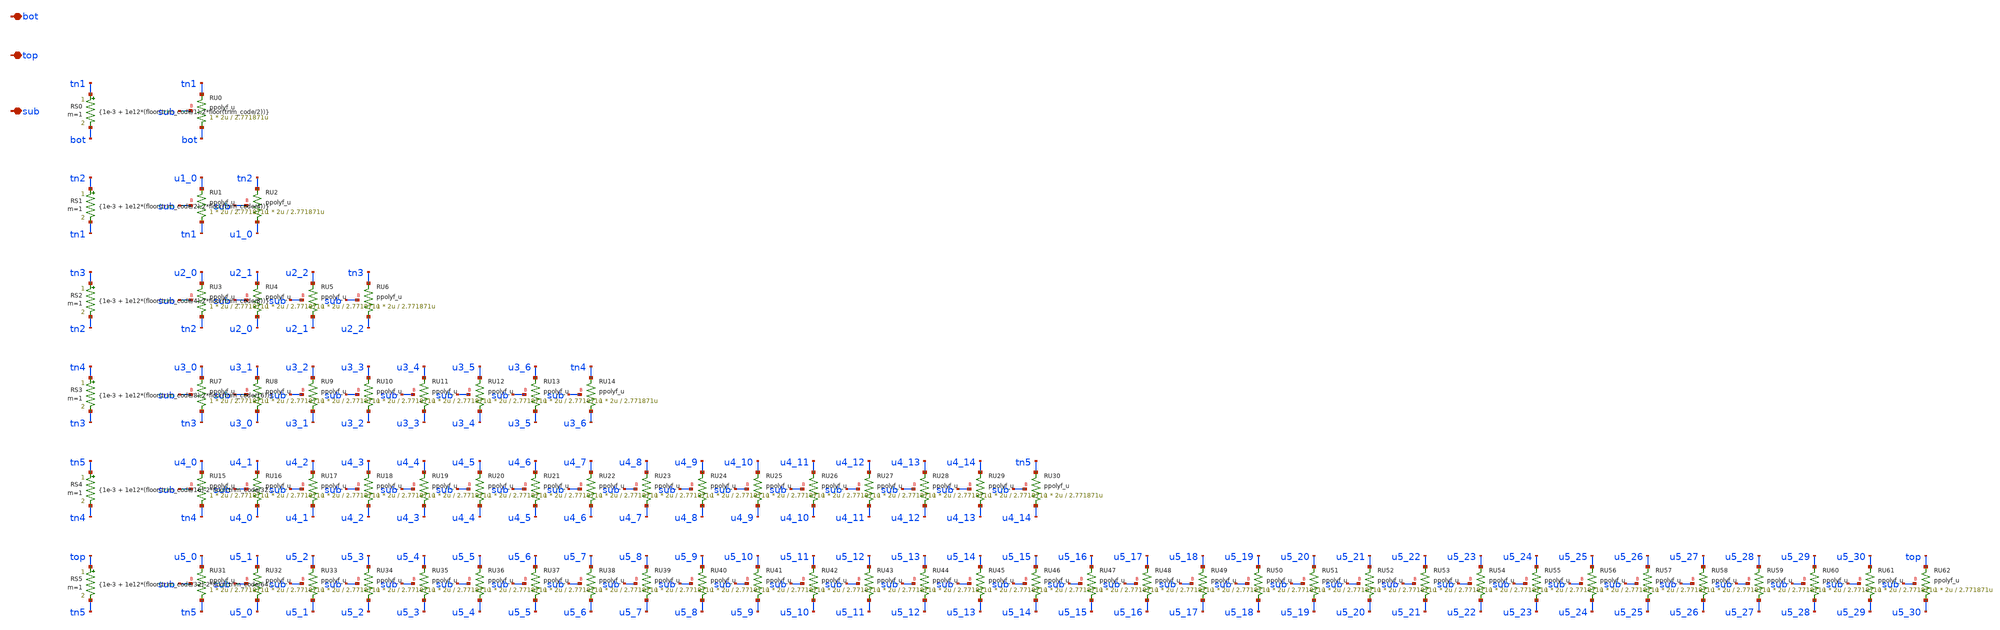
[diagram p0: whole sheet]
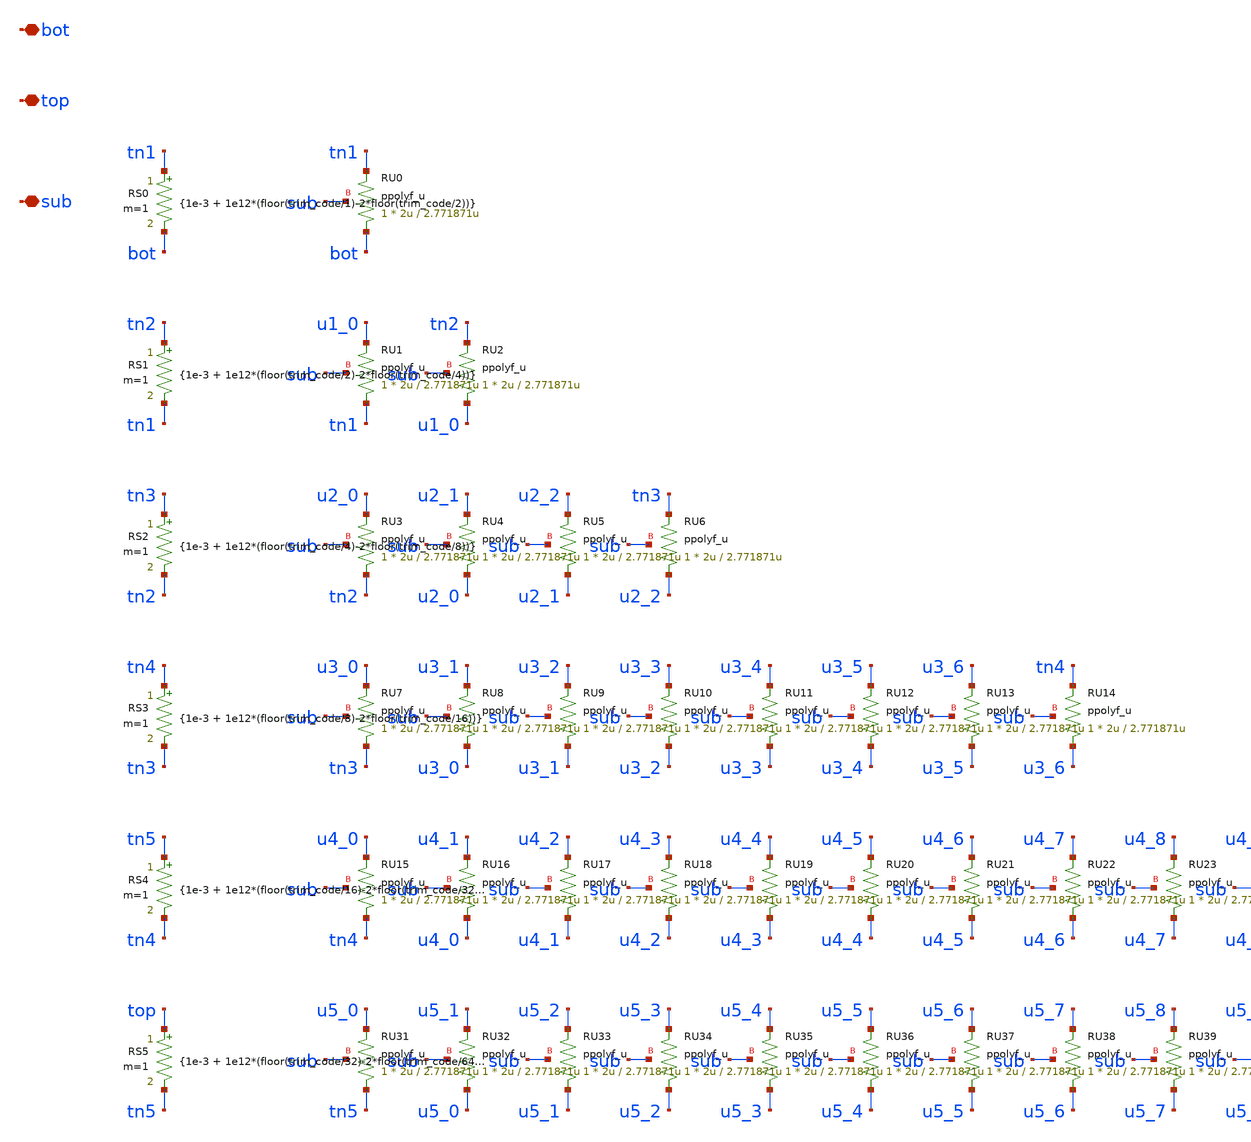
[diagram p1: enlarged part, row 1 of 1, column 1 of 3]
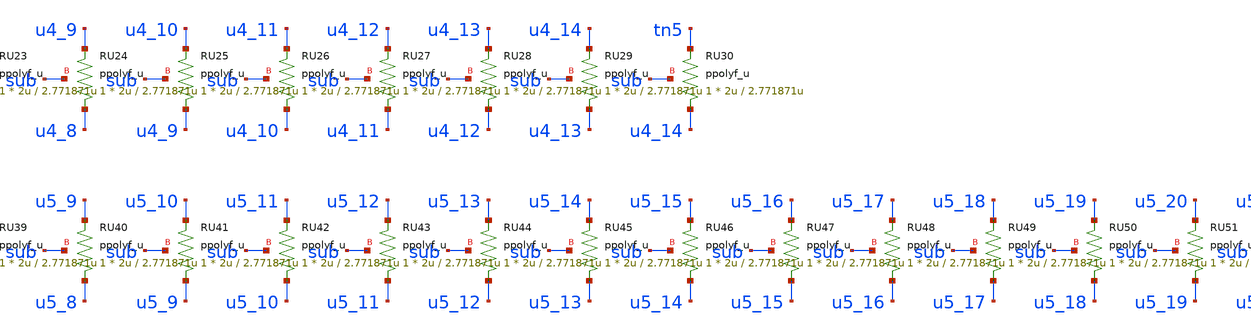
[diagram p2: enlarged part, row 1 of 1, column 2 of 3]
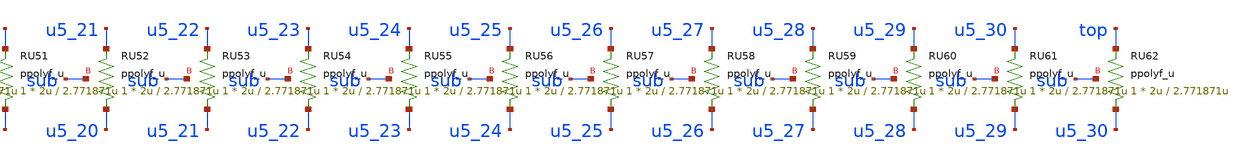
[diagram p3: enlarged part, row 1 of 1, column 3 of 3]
** sch_path: design/bandgap_trim.sch

.param trim_code=32

**.subckt bandgap_trim bot top sub
*.iopin bot
*.iopin top
*.iopin sub
XRU0 bot tn1 sub ppolyf_u r_width=2u r_length=2.771871u m=1
RS0 tn1 bot {1e-3 + 1e12*(floor(trim_code/1)-2*floor(trim_code/2))} m=1
XRU1 tn1 u1_0 sub ppolyf_u r_width=2u r_length=2.771871u m=1
XRU2 u1_0 tn2 sub ppolyf_u r_width=2u r_length=2.771871u m=1
RS1 tn2 tn1 {1e-3 + 1e12*(floor(trim_code/2)-2*floor(trim_code/4))} m=1
XRU3 tn2 u2_0 sub ppolyf_u r_width=2u r_length=2.771871u m=1
XRU4 u2_0 u2_1 sub ppolyf_u r_width=2u r_length=2.771871u m=1
XRU5 u2_1 u2_2 sub ppolyf_u r_width=2u r_length=2.771871u m=1
XRU6 u2_2 tn3 sub ppolyf_u r_width=2u r_length=2.771871u m=1
RS2 tn3 tn2 {1e-3 + 1e12*(floor(trim_code/4)-2*floor(trim_code/8))} m=1
XRU7 tn3 u3_0 sub ppolyf_u r_width=2u r_length=2.771871u m=1
XRU8 u3_0 u3_1 sub ppolyf_u r_width=2u r_length=2.771871u m=1
XRU9 u3_1 u3_2 sub ppolyf_u r_width=2u r_length=2.771871u m=1
XRU10 u3_2 u3_3 sub ppolyf_u r_width=2u r_length=2.771871u m=1
XRU11 u3_3 u3_4 sub ppolyf_u r_width=2u r_length=2.771871u m=1
XRU12 u3_4 u3_5 sub ppolyf_u r_width=2u r_length=2.771871u m=1
XRU13 u3_5 u3_6 sub ppolyf_u r_width=2u r_length=2.771871u m=1
XRU14 u3_6 tn4 sub ppolyf_u r_width=2u r_length=2.771871u m=1
RS3 tn4 tn3 {1e-3 + 1e12*(floor(trim_code/8)-2*floor(trim_code/16))} m=1
XRU15 tn4 u4_0 sub ppolyf_u r_width=2u r_length=2.771871u m=1
XRU16 u4_0 u4_1 sub ppolyf_u r_width=2u r_length=2.771871u m=1
XRU17 u4_1 u4_2 sub ppolyf_u r_width=2u r_length=2.771871u m=1
XRU18 u4_2 u4_3 sub ppolyf_u r_width=2u r_length=2.771871u m=1
XRU19 u4_3 u4_4 sub ppolyf_u r_width=2u r_length=2.771871u m=1
XRU20 u4_4 u4_5 sub ppolyf_u r_width=2u r_length=2.771871u m=1
XRU21 u4_5 u4_6 sub ppolyf_u r_width=2u r_length=2.771871u m=1
XRU22 u4_6 u4_7 sub ppolyf_u r_width=2u r_length=2.771871u m=1
XRU23 u4_7 u4_8 sub ppolyf_u r_width=2u r_length=2.771871u m=1
XRU24 u4_8 u4_9 sub ppolyf_u r_width=2u r_length=2.771871u m=1
XRU25 u4_9 u4_10 sub ppolyf_u r_width=2u r_length=2.771871u m=1
XRU26 u4_10 u4_11 sub ppolyf_u r_width=2u r_length=2.771871u m=1
XRU27 u4_11 u4_12 sub ppolyf_u r_width=2u r_length=2.771871u m=1
XRU28 u4_12 u4_13 sub ppolyf_u r_width=2u r_length=2.771871u m=1
XRU29 u4_13 u4_14 sub ppolyf_u r_width=2u r_length=2.771871u m=1
XRU30 u4_14 tn5 sub ppolyf_u r_width=2u r_length=2.771871u m=1
RS4 tn5 tn4 {1e-3 + 1e12*(floor(trim_code/16)-2*floor(trim_code/32))} m=1
XRU31 tn5 u5_0 sub ppolyf_u r_width=2u r_length=2.771871u m=1
XRU32 u5_0 u5_1 sub ppolyf_u r_width=2u r_length=2.771871u m=1
XRU33 u5_1 u5_2 sub ppolyf_u r_width=2u r_length=2.771871u m=1
XRU34 u5_2 u5_3 sub ppolyf_u r_width=2u r_length=2.771871u m=1
XRU35 u5_3 u5_4 sub ppolyf_u r_width=2u r_length=2.771871u m=1
XRU36 u5_4 u5_5 sub ppolyf_u r_width=2u r_length=2.771871u m=1
XRU37 u5_5 u5_6 sub ppolyf_u r_width=2u r_length=2.771871u m=1
XRU38 u5_6 u5_7 sub ppolyf_u r_width=2u r_length=2.771871u m=1
XRU39 u5_7 u5_8 sub ppolyf_u r_width=2u r_length=2.771871u m=1
XRU40 u5_8 u5_9 sub ppolyf_u r_width=2u r_length=2.771871u m=1
XRU41 u5_9 u5_10 sub ppolyf_u r_width=2u r_length=2.771871u m=1
XRU42 u5_10 u5_11 sub ppolyf_u r_width=2u r_length=2.771871u m=1
XRU43 u5_11 u5_12 sub ppolyf_u r_width=2u r_length=2.771871u m=1
XRU44 u5_12 u5_13 sub ppolyf_u r_width=2u r_length=2.771871u m=1
XRU45 u5_13 u5_14 sub ppolyf_u r_width=2u r_length=2.771871u m=1
XRU46 u5_14 u5_15 sub ppolyf_u r_width=2u r_length=2.771871u m=1
XRU47 u5_15 u5_16 sub ppolyf_u r_width=2u r_length=2.771871u m=1
XRU48 u5_16 u5_17 sub ppolyf_u r_width=2u r_length=2.771871u m=1
XRU49 u5_17 u5_18 sub ppolyf_u r_width=2u r_length=2.771871u m=1
XRU50 u5_18 u5_19 sub ppolyf_u r_width=2u r_length=2.771871u m=1
XRU51 u5_19 u5_20 sub ppolyf_u r_width=2u r_length=2.771871u m=1
XRU52 u5_20 u5_21 sub ppolyf_u r_width=2u r_length=2.771871u m=1
XRU53 u5_21 u5_22 sub ppolyf_u r_width=2u r_length=2.771871u m=1
XRU54 u5_22 u5_23 sub ppolyf_u r_width=2u r_length=2.771871u m=1
XRU55 u5_23 u5_24 sub ppolyf_u r_width=2u r_length=2.771871u m=1
XRU56 u5_24 u5_25 sub ppolyf_u r_width=2u r_length=2.771871u m=1
XRU57 u5_25 u5_26 sub ppolyf_u r_width=2u r_length=2.771871u m=1
XRU58 u5_26 u5_27 sub ppolyf_u r_width=2u r_length=2.771871u m=1
XRU59 u5_27 u5_28 sub ppolyf_u r_width=2u r_length=2.771871u m=1
XRU60 u5_28 u5_29 sub ppolyf_u r_width=2u r_length=2.771871u m=1
XRU61 u5_29 u5_30 sub ppolyf_u r_width=2u r_length=2.771871u m=1
XRU62 u5_30 top sub ppolyf_u r_width=2u r_length=2.771871u m=1
RS5 top tn5 {1e-3 + 1e12*(floor(trim_code/32)-2*floor(trim_code/64))} m=1
**.ends
.end
